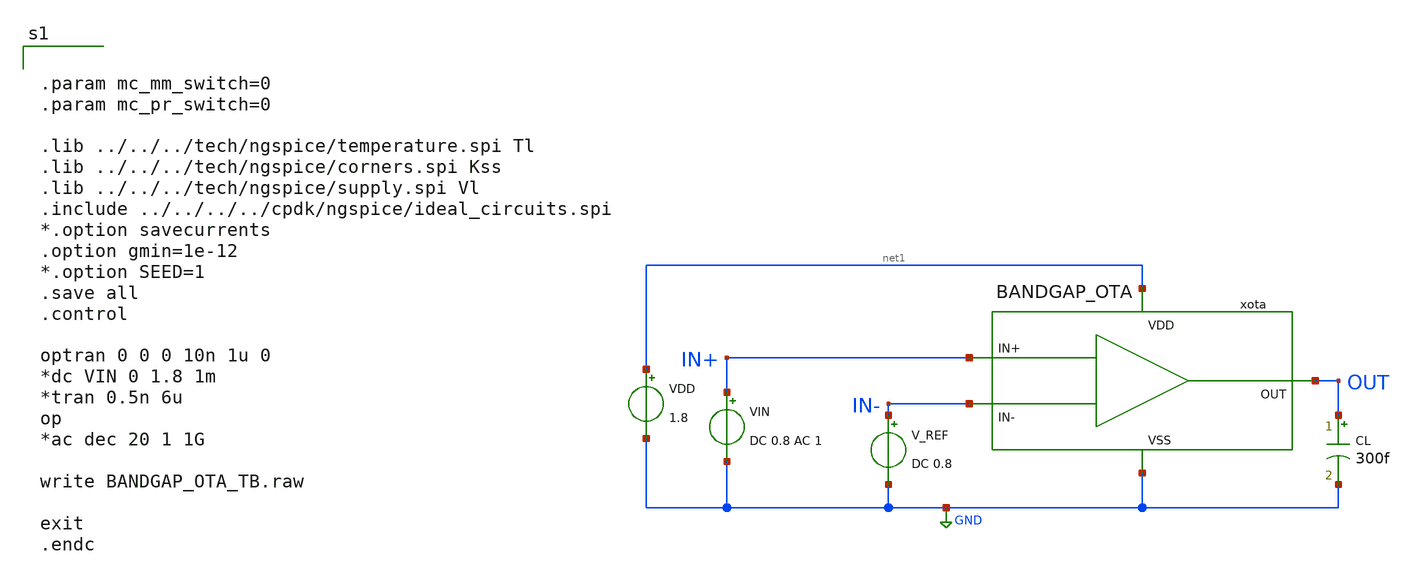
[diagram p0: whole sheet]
** sch_path: design/LELO_GR03_SKY130A/BANDGAP_OTA_TB.sch
**.subckt BANDGAP_OTA_TB
xota net1 IN+ OUT IN- GND BANDGAP_OTA
CL OUT GND 300f m=1
VIN IN+ GND DC 0.8 AC 1
V_REF IN- GND DC 0.8
VDD net1 GND 1.8
**** begin user architecture code


.param mc_mm_switch=0
.param mc_pr_switch=0

.lib ../../../tech/ngspice/temperature.spi Tl
.lib ../../../tech/ngspice/corners.spi Kss
.lib ../../../tech/ngspice/supply.spi Vl
.include ../../../../cpdk/ngspice/ideal_circuits.spi
*.option savecurrents
.option gmin=1e-12
*.option SEED=1
.save all
.control

optran 0 0 0 10n 1u 0
*dc VIN 0 1.8 1m
*tran 0.5n 6u
op
*ac dec 20 1 1G

write BANDGAP_OTA_TB.raw

exit
.endc


**** end user architecture code
**.ends
.GLOBAL GND
.end
